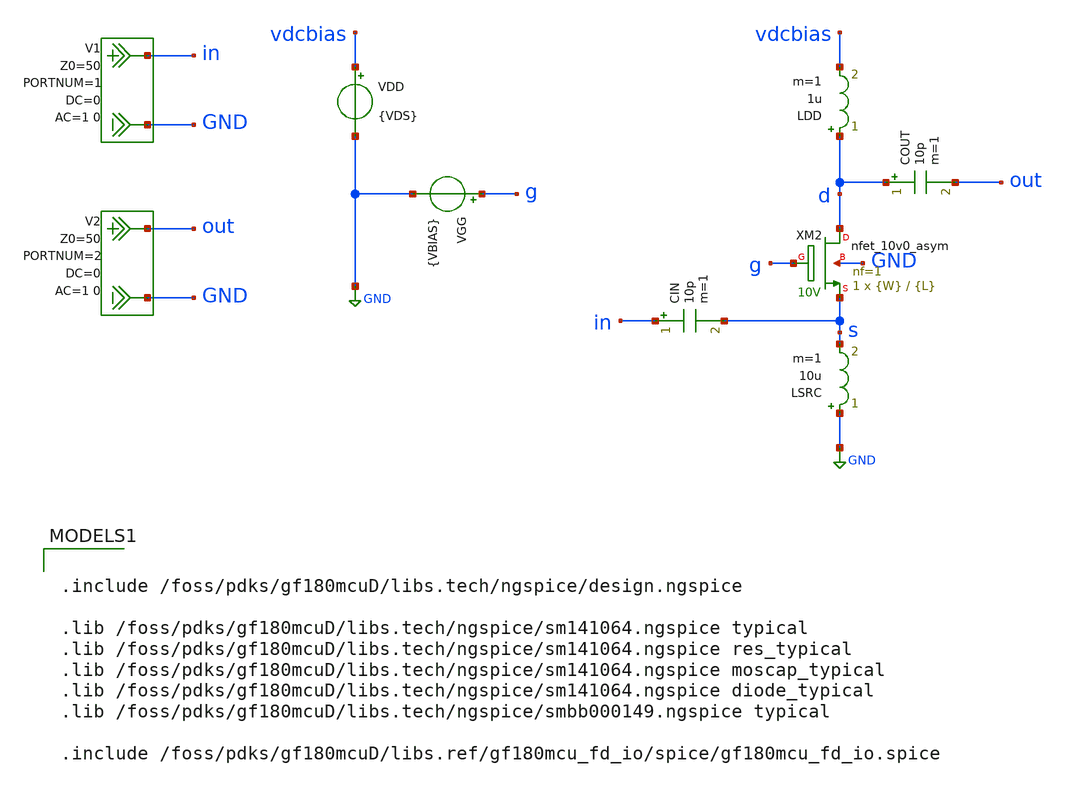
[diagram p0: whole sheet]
** sch_path: NFmin_Simulation/simulations/10v0/nfmin_jd_nmos_cg_10.sch
**.subckt nfmin_jd_nmos_cg_10
VGG g GND {VBIAS}
VDD vdcbias GND {VDS}
LDD d vdcbias 1u m=1
COUT d out 10p m=1
CIN in s 10p m=1
V1 in GND DC 0 AC 1 0 portnum 1 z0 50
V2 out GND DC 0 AC 1 0 portnum 2 z0 50
LSRC GND s 10u m=1
XM2 d g s GND nfet_10v0_asym L={L} W={W} nf=1 ad='W * 1.48u' as='W * 0.48u' pd='2 * (W + 1.48u)' ps='2 * (W + 0.48u)'
+ nrd=0 nrs=0 sa=0 sb=0 sd=0 m=1
**** begin user architecture code



.option savecurrents

.param fnoicor=0
.param sw_stat_mismatch=0

* ============================================================
* nfet_10v0_asym common-gate LNA device characterization
*
* Device note:
*   nfet_10v0_asym is an asymmetric 10 V LDNMOS.
*   Keep drain/source orientation correct:
*     drain  = high-voltage drain side
*     source = RF input source side, DC near GND through LSRC
*
* Testbench assumption:
*   Gate DC   = VBIAS
*   Source DC = near GND through LSRC
*   Drain DC  = near VDS through RF choke
*
* Therefore:
*   VGS = approximately VBIAS
*   VDS = approximately selected VDS
*
* Nominal comparison sweep:
*   VDS = 5.0 V fixed
*   W   = 4, 5, 10, 20, 50 um
*   L   = 0.60, 0.70, 1.00 um
*   VGS = 0.50 V to 2.50 V in 5 mV steps
*
* Total points:
*   1 x 5 x 3 x 401 = 6015 points
*
* Note:
*   Do not use W = 0.30 um or 1 um for this 10 V LDNMOS sweep.
* ============================================================

.param VBIAS=0.9
.param VDS=5.0

.param W=4.00e-6
.param L=0.60e-6

.control
  set noaskquit

  echo VDS_set_V W_m L_m VBIAS_set_V VGS_actual_V VDS_actual_V VBS_actual_V ID_A JD_mA_per_um Pdc_mW
+ gm_S gds_S gm_ID_1_per_V ro_Ohm gmro inv_gm_Ohm NFmin_dB NF_dB Rn_Ohm SOpt_real SOpt_imag SOpt_mag >
+ nmos10_cg_full_nom5v.txt

  foreach vdsval 5.0

    foreach wval 4e-6 5e-6 10e-6 20e-6 50e-6

      foreach lval 0.60e-6 0.70e-6 1.00e-6

        setplot const
        let k = 0

        while k <= 400

          setplot const
          let vgs = 0.50 + 0.005*k

          alterparam VDS = $vdsval
          alterparam W = $wval
          alterparam L = $lval
          alterparam VBIAS = $&vgs
          reset

          op

          let idn_tmp = abs(i(vdd))
          let jd_tmp = 1e-3*idn_tmp/$wval
          let pdc_tmp = 1e3*idn_tmp*$vdsval

          let vgs_tmp = v(g)-v(s)
          let vds_tmp = v(d)-v(s)
          let vbs_tmp = -v(s)

          let gm_tmp = @m.xm2.m0[gm]
          let gds_tmp = @m.xm2.m0[gds]

          let gm_id_tmp = gm_tmp/idn_tmp
          let ro_tmp = 1/gds_tmp
          let gmro_tmp = gm_tmp/gds_tmp
          let inv_gm_tmp = 1/gm_tmp

          set idn_op = $&idn_tmp
          set jd_op = $&jd_tmp
          set pdc_op = $&pdc_tmp
          set vgs_op = $&vgs_tmp
          set vds_op = $&vds_tmp
          set vbs_op = $&vbs_tmp
          set gm_op = $&gm_tmp
          set gds_op = $&gds_tmp
          set gm_id_op = $&gm_id_tmp
          set ro_op = $&ro_tmp
          set gmro_op = $&gmro_tmp
          set inv_gm_op = $&inv_gm_tmp

          destroy $curplot

          sp lin 1 2.4e9 2.4e9 1

          let nfmin_val = real(NFmin)
          let nf_val = real(NF)
          let rn_val = real(Rn)
          let sopt_re = real(SOpt)
          let sopt_im = imag(SOpt)
          let sopt_mag = sqrt(sopt_re*sopt_re + sopt_im*sopt_im)

          echo $vdsval $wval $lval $&vgs $vgs_op $vds_op $vbs_op $idn_op $jd_op $pdc_op $gm_op
+ $gds_op $gm_id_op $ro_op $gmro_op $inv_gm_op $&nfmin_val $&nf_val $&rn_val $&sopt_re $&sopt_im $&sopt_mag
+ >> nmos10_cg_full_nom5v.txt

          destroy $curplot

          setplot const
          let k = k + 1

        end

      end

    end

  end

.endc



.include /foss/pdks/gf180mcuD/libs.tech/ngspice/design.ngspice

.lib /foss/pdks/gf180mcuD/libs.tech/ngspice/sm141064.ngspice typical
.lib /foss/pdks/gf180mcuD/libs.tech/ngspice/sm141064.ngspice res_typical
.lib /foss/pdks/gf180mcuD/libs.tech/ngspice/sm141064.ngspice moscap_typical
.lib /foss/pdks/gf180mcuD/libs.tech/ngspice/sm141064.ngspice diode_typical
.lib /foss/pdks/gf180mcuD/libs.tech/ngspice/smbb000149.ngspice typical

.include /foss/pdks/gf180mcuD/libs.ref/gf180mcu_fd_io/spice/gf180mcu_fd_io.spice

**** end user architecture code
**.ends
.GLOBAL GND
.end
